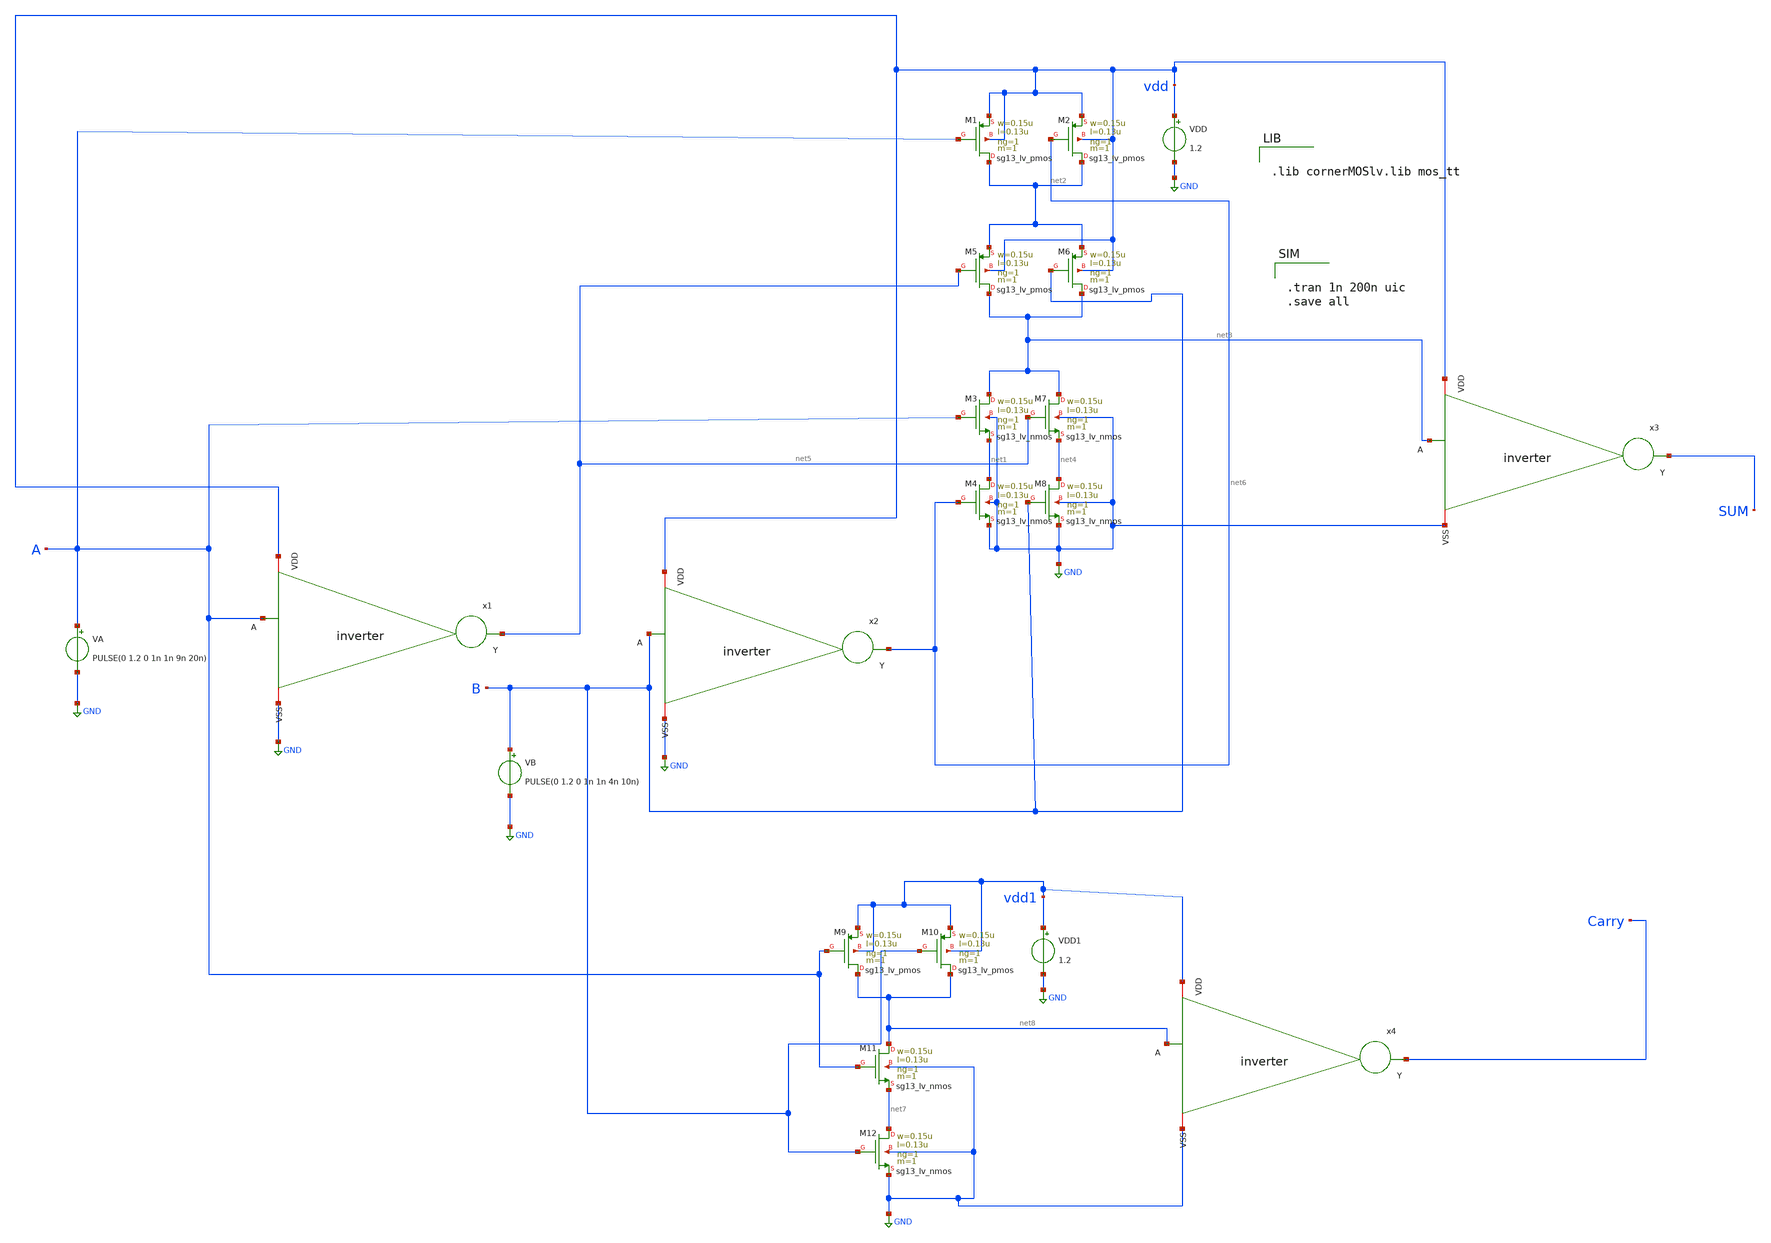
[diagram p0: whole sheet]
** sch_path: half-adder.sch
**.subckt half-adder
XM1 net2 A vdd vdd sg13_lv_pmos w=0.15u l=0.13u ng=1 m=1 mm_ok=1
XM2 net2 net6 vdd vdd sg13_lv_pmos w=0.15u l=0.13u ng=1 m=1 mm_ok=1
XM3 net3 A net1 GND sg13_lv_nmos w=0.15u l=0.13u ng=1 m=1 mm_ok=1
XM4 net1 net6 GND GND sg13_lv_nmos w=0.15u l=0.13u ng=1 m=1 mm_ok=1
VDD vdd GND 1.2
VA A GND PULSE(0 1.2 0 1n 1n 9n 20n)
VB B GND PULSE(0 1.2 0 1n 1n 4n 10n)
XM5 net3 net5 net2 vdd sg13_lv_pmos w=0.15u l=0.13u ng=1 m=1 mm_ok=1
XM6 net3 B net2 vdd sg13_lv_pmos w=0.15u l=0.13u ng=1 m=1 mm_ok=1
XM7 net3 net5 net4 GND sg13_lv_nmos w=0.15u l=0.13u ng=1 m=1 mm_ok=1
XM8 net4 B GND GND sg13_lv_nmos w=0.15u l=0.13u ng=1 m=1 mm_ok=1
x1 vdd A net5 GND inverter
x2 vdd B net6 GND inverter
x3 vdd net3 SUM GND inverter
XM9 net8 A vdd1 vdd1 sg13_lv_pmos w=0.15u l=0.13u ng=1 m=1 mm_ok=1
XM10 net8 B vdd1 vdd1 sg13_lv_pmos w=0.15u l=0.13u ng=1 m=1 mm_ok=1
XM11 net8 A net7 GND sg13_lv_nmos w=0.15u l=0.13u ng=1 m=1 mm_ok=1
XM12 net7 B GND GND sg13_lv_nmos w=0.15u l=0.13u ng=1 m=1 mm_ok=1
VDD1 vdd1 GND 1.2
x4 vdd1 net8 Carry GND inverter
**** begin user architecture code


.lib cornerMOSlv.lib mos_tt



.tran 1n 200n uic
.save all


**** end user architecture code
**.ends

* expanding   symbol:  xchem/xchem/inverter.sym # of pins=4
** sym_path: inverter.sym
** sch_path: inverter.sch
.subckt inverter VDD A Y VSS
*.ipin A
*.iopin VDD
*.iopin VSS
*.opin Y
XM1 Y A VDD VDD sg13_lv_pmos w=0.15u l=0.13u ng=1 m=1 mm_ok=1
XM2 Y A VSS VSS sg13_lv_nmos w=0.15u l=0.13u ng=1 m=1 mm_ok=1
.ends

.GLOBAL GND
.end
